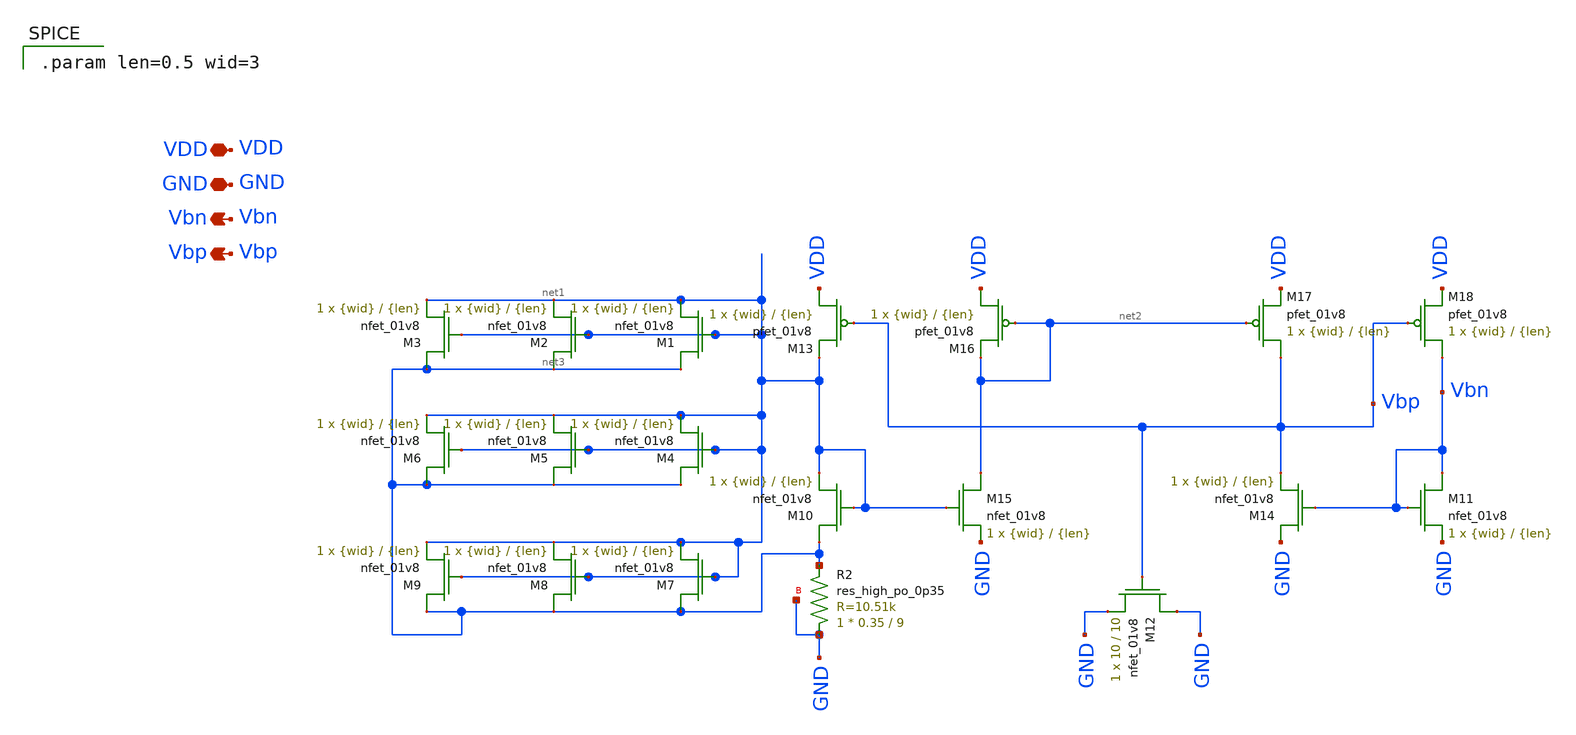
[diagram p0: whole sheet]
** sch_path: final/LDS/bias_gen_LDS.sch
**.subckt bias_gen_LDS VDD Vbp GND Vbn
*.iopin VDD
*.opin Vbp
*.iopin GND
*.opin Vbn
XM10 net3 net1 net1 GND sky130_fd_pr__nfet_01v8 L={len} W={wid} nf=1 ad='int((nf+1)/2) * W/nf * 0.29'
+ as='int((nf+2)/2) * W/nf * 0.29' pd='2*int((nf+1)/2) * (W/nf + 0.29)' ps='2*int((nf+2)/2) * (W/nf + 0.29)'
+ nrd='0.29 / W' nrs='0.29 / W' sa=0 sb=0 sd=0 mult=1 m=1
XM11 Vbn Vbn GND GND sky130_fd_pr__nfet_01v8 L={len} W={wid} nf=1 ad='int((nf+1)/2) * W/nf * 0.29' as='int((nf+2)/2) * W/nf * 0.29'
+ pd='2*int((nf+1)/2) * (W/nf + 0.29)' ps='2*int((nf+2)/2) * (W/nf + 0.29)' nrd='0.29 / W' nrs='0.29 / W'
+ sa=0 sb=0 sd=0 mult=1 m=1
XM12 GND Vbp GND GND sky130_fd_pr__nfet_01v8 L=10 W=10 nf=1 ad='int((nf+1)/2) * W/nf * 0.29' as='int((nf+2)/2) * W/nf * 0.29'
+ pd='2*int((nf+1)/2) * (W/nf + 0.29)' ps='2*int((nf+2)/2) * (W/nf + 0.29)' nrd='0.29 / W' nrs='0.29 / W'
+ sa=0 sb=0 sd=0 mult=1 m=1
XM13 VDD Vbp net1 VDD sky130_fd_pr__pfet_01v8 L={len} W={wid} nf=1 ad='int((nf+1)/2) * W/nf * 0.29' as='int((nf+2)/2) * W/nf * 0.29'
+ pd='2*int((nf+1)/2) * (W/nf + 0.29)' ps='2*int((nf+2)/2) * (W/nf + 0.29)' nrd='0.29 / W' nrs='0.29 / W'
+ sa=0 sb=0 sd=0 mult=1 m=1
XM14 GND Vbn Vbp GND sky130_fd_pr__nfet_01v8 L={len} W={wid} nf=1 ad='int((nf+1)/2) * W/nf * 0.29' as='int((nf+2)/2) * W/nf * 0.29'
+ pd='2*int((nf+1)/2) * (W/nf + 0.29)' ps='2*int((nf+2)/2) * (W/nf + 0.29)' nrd='0.29 / W' nrs='0.29 / W'
+ sa=0 sb=0 sd=0 mult=1 m=1
XM15 net2 net1 GND GND sky130_fd_pr__nfet_01v8 L={len} W={wid} nf=1 ad='int((nf+1)/2) * W/nf * 0.29'
+ as='int((nf+2)/2) * W/nf * 0.29' pd='2*int((nf+1)/2) * (W/nf + 0.29)' ps='2*int((nf+2)/2) * (W/nf + 0.29)'
+ nrd='0.29 / W' nrs='0.29 / W' sa=0 sb=0 sd=0 mult=1 m=1
XM16 VDD net2 net2 VDD sky130_fd_pr__pfet_01v8 L={len} W={wid} nf=1 ad='int((nf+1)/2) * W/nf * 0.29'
+ as='int((nf+2)/2) * W/nf * 0.29' pd='2*int((nf+1)/2) * (W/nf + 0.29)' ps='2*int((nf+2)/2) * (W/nf + 0.29)'
+ nrd='0.29 / W' nrs='0.29 / W' sa=0 sb=0 sd=0 mult=1 m=1
XM17 Vbp net2 VDD VDD sky130_fd_pr__pfet_01v8 L={len} W={wid} nf=1 ad='int((nf+1)/2) * W/nf * 0.29' as='int((nf+2)/2) * W/nf * 0.29'
+ pd='2*int((nf+1)/2) * (W/nf + 0.29)' ps='2*int((nf+2)/2) * (W/nf + 0.29)' nrd='0.29 / W' nrs='0.29 / W'
+ sa=0 sb=0 sd=0 mult=1 m=1
XM18 Vbn Vbp VDD VDD sky130_fd_pr__pfet_01v8 L={len} W={wid} nf=1 ad='int((nf+1)/2) * W/nf * 0.29' as='int((nf+2)/2) * W/nf * 0.29'
+ pd='2*int((nf+1)/2) * (W/nf + 0.29)' ps='2*int((nf+2)/2) * (W/nf + 0.29)' nrd='0.29 / W' nrs='0.29 / W'
+ sa=0 sb=0 sd=0 mult=1 m=1
XR2 GND net3 GND sky130_fd_pr__res_high_po_0p35 L=9 mult=1 m=1
XM1 net3 net1 net1 GND sky130_fd_pr__nfet_01v8 L={len} W={wid} nf=1 ad='int((nf+1)/2) * W/nf * 0.29'
+ as='int((nf+2)/2) * W/nf * 0.29' pd='2*int((nf+1)/2) * (W/nf + 0.29)' ps='2*int((nf+2)/2) * (W/nf + 0.29)'
+ nrd='0.29 / W' nrs='0.29 / W' sa=0 sb=0 sd=0 mult=1 m=1
XM2 net3 net1 net1 GND sky130_fd_pr__nfet_01v8 L={len} W={wid} nf=1 ad='int((nf+1)/2) * W/nf * 0.29'
+ as='int((nf+2)/2) * W/nf * 0.29' pd='2*int((nf+1)/2) * (W/nf + 0.29)' ps='2*int((nf+2)/2) * (W/nf + 0.29)'
+ nrd='0.29 / W' nrs='0.29 / W' sa=0 sb=0 sd=0 mult=1 m=1
XM3 net3 net1 net1 GND sky130_fd_pr__nfet_01v8 L={len} W={wid} nf=1 ad='int((nf+1)/2) * W/nf * 0.29'
+ as='int((nf+2)/2) * W/nf * 0.29' pd='2*int((nf+1)/2) * (W/nf + 0.29)' ps='2*int((nf+2)/2) * (W/nf + 0.29)'
+ nrd='0.29 / W' nrs='0.29 / W' sa=0 sb=0 sd=0 mult=1 m=1
XM4 net3 net1 net1 GND sky130_fd_pr__nfet_01v8 L={len} W={wid} nf=1 ad='int((nf+1)/2) * W/nf * 0.29'
+ as='int((nf+2)/2) * W/nf * 0.29' pd='2*int((nf+1)/2) * (W/nf + 0.29)' ps='2*int((nf+2)/2) * (W/nf + 0.29)'
+ nrd='0.29 / W' nrs='0.29 / W' sa=0 sb=0 sd=0 mult=1 m=1
XM5 net3 net1 net1 GND sky130_fd_pr__nfet_01v8 L={len} W={wid} nf=1 ad='int((nf+1)/2) * W/nf * 0.29'
+ as='int((nf+2)/2) * W/nf * 0.29' pd='2*int((nf+1)/2) * (W/nf + 0.29)' ps='2*int((nf+2)/2) * (W/nf + 0.29)'
+ nrd='0.29 / W' nrs='0.29 / W' sa=0 sb=0 sd=0 mult=1 m=1
XM6 net3 net1 net1 GND sky130_fd_pr__nfet_01v8 L={len} W={wid} nf=1 ad='int((nf+1)/2) * W/nf * 0.29'
+ as='int((nf+2)/2) * W/nf * 0.29' pd='2*int((nf+1)/2) * (W/nf + 0.29)' ps='2*int((nf+2)/2) * (W/nf + 0.29)'
+ nrd='0.29 / W' nrs='0.29 / W' sa=0 sb=0 sd=0 mult=1 m=1
XM7 net3 net1 net1 GND sky130_fd_pr__nfet_01v8 L={len} W={wid} nf=1 ad='int((nf+1)/2) * W/nf * 0.29'
+ as='int((nf+2)/2) * W/nf * 0.29' pd='2*int((nf+1)/2) * (W/nf + 0.29)' ps='2*int((nf+2)/2) * (W/nf + 0.29)'
+ nrd='0.29 / W' nrs='0.29 / W' sa=0 sb=0 sd=0 mult=1 m=1
XM8 net3 net1 net1 GND sky130_fd_pr__nfet_01v8 L={len} W={wid} nf=1 ad='int((nf+1)/2) * W/nf * 0.29'
+ as='int((nf+2)/2) * W/nf * 0.29' pd='2*int((nf+1)/2) * (W/nf + 0.29)' ps='2*int((nf+2)/2) * (W/nf + 0.29)'
+ nrd='0.29 / W' nrs='0.29 / W' sa=0 sb=0 sd=0 mult=1 m=1
XM9 net3 net1 net1 GND sky130_fd_pr__nfet_01v8 L={len} W={wid} nf=1 ad='int((nf+1)/2) * W/nf * 0.29'
+ as='int((nf+2)/2) * W/nf * 0.29' pd='2*int((nf+1)/2) * (W/nf + 0.29)' ps='2*int((nf+2)/2) * (W/nf + 0.29)'
+ nrd='0.29 / W' nrs='0.29 / W' sa=0 sb=0 sd=0 mult=1 m=1
**** begin user architecture code

.param len=0.5 wid=3

**** end user architecture code
**.ends
.end
